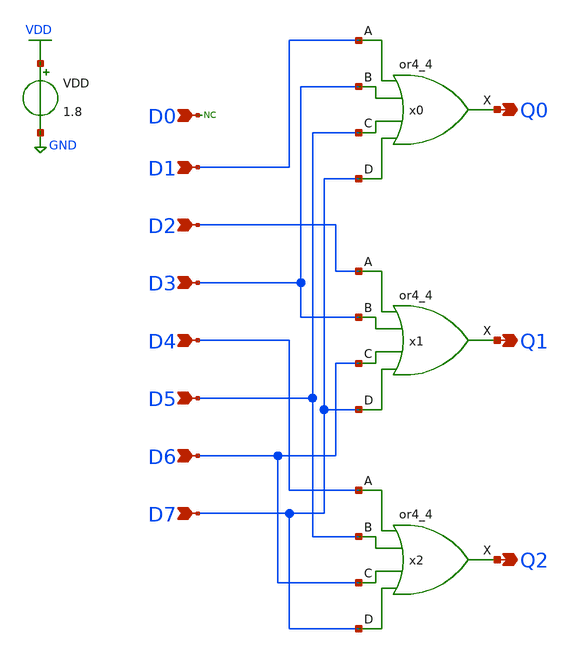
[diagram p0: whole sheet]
** sch_path: PriorityEncoder/Priority_Encoder_v0p0p1.sch
.lib $::SKYWATER_MODELS/sky130.lib.spice tt
.include $::SKYWATER_STDCELLS/sky130_fd_sc_hd.spice

**.subckt Priority_Encoder_v0p0p1 D2 D3 D4 D5 D6 D7 D1 D0 Q0 Q1 Q2
*.ipin D2
*.ipin D3
*.ipin D4
*.ipin D5
*.ipin D6
*.ipin D7
*.ipin D1
*.ipin D0
*.opin Q0
*.opin Q1
*.opin Q2
x0 D1 D3 D5 D7 GND GND VDD VDD Q0 sky130_fd_sc_hd__or4_4
x1 D2 D3 D6 D7 GND GND VDD VDD Q1 sky130_fd_sc_hd__or4_4
x2 D4 D5 D6 D7 GND GND VDD VDD Q2 sky130_fd_sc_hd__or4_4
VDD VDD GND 1.8
* noconn D0
**.ends
.GLOBAL VDD
.GLOBAL GND
.end
